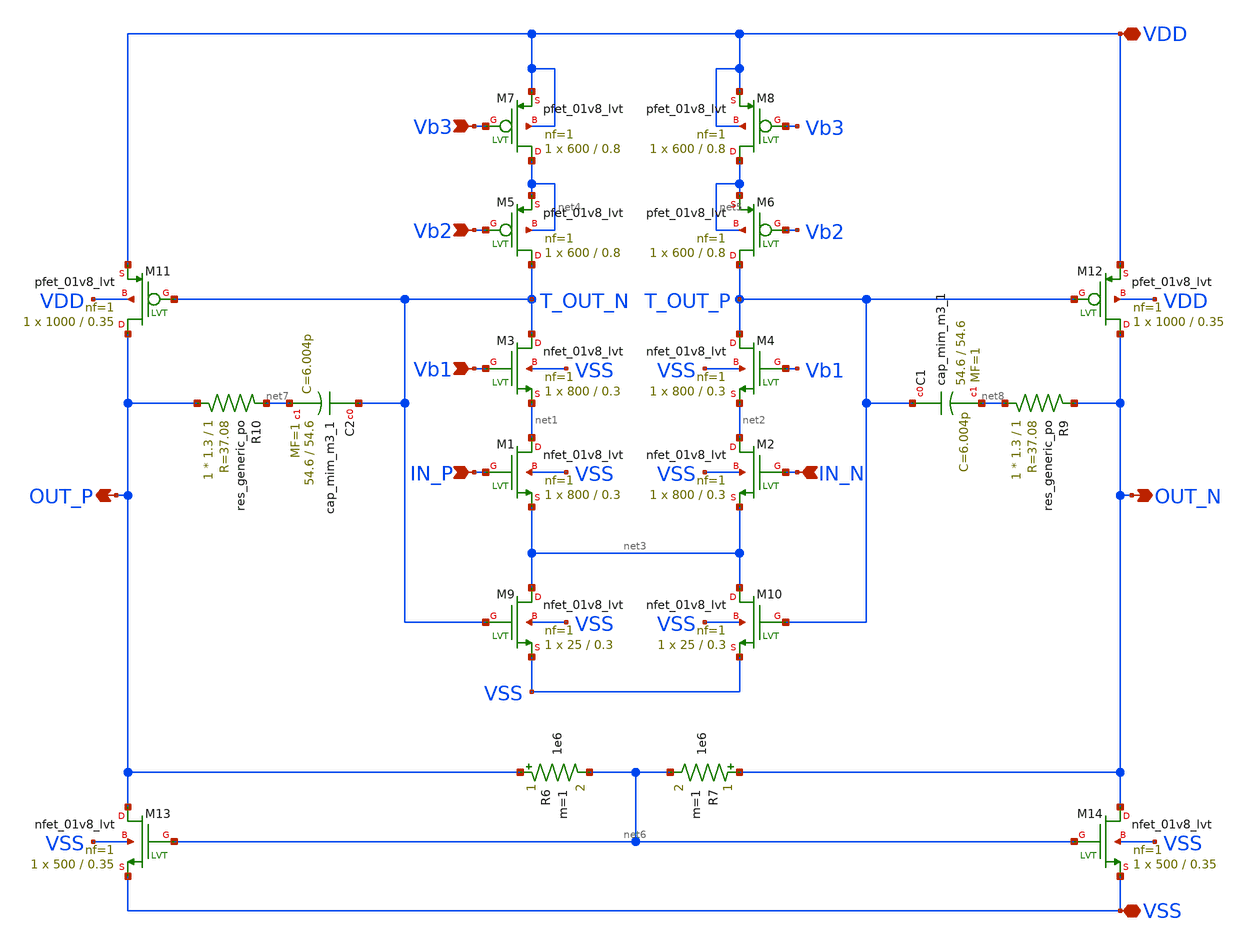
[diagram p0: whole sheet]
** sch_path: xschem/two_stage_amplifier.sch
**.subckt two_stage_amplifier VSS VDD Vb1 Vb2 Vb3 IN_P IN_N OUT_N OUT_P
*.iopin VSS
*.iopin VDD
*.ipin Vb1
*.ipin Vb2
*.ipin Vb3
*.ipin IN_P
*.ipin IN_N
*.opin OUT_N
*.opin OUT_P
XM1 net1 IN_P net3 VSS sky130_fd_pr__nfet_01v8_lvt L=0.3 W=800 nf=1 ad='int((1 + 1)/2) * 800 / 1 * 0.29'
+ as='int((1 + 2)/2) * 800 / 1 * 0.29' pd='2*int((1 + 1)/2) * (800 / 1 + 0.29)' ps='2*int((1 + 2)/2) * (800 / 1 + 0.29)'
+ nrd='0.29 / 800 ' nrs='0.29 / 800 ' sa=0 sb=0 sd=0 mult=1 m=1
XM2 net2 IN_N net3 VSS sky130_fd_pr__nfet_01v8_lvt L=0.3 W=800 nf=1 ad='int((1 + 1)/2) * 800 / 1 * 0.29'
+ as='int((1 + 2)/2) * 800 / 1 * 0.29' pd='2*int((1 + 1)/2) * (800 / 1 + 0.29)' ps='2*int((1 + 2)/2) * (800 / 1 + 0.29)'
+ nrd='0.29 / 800 ' nrs='0.29 / 800 ' sa=0 sb=0 sd=0 mult=1 m=1
XM3 T_OUT_N Vb1 net1 VSS sky130_fd_pr__nfet_01v8_lvt L=0.3 W=800 nf=1 ad='int((1 + 1)/2) * 800 / 1 * 0.29'
+ as='int((1 + 2)/2) * 800 / 1 * 0.29' pd='2*int((1 + 1)/2) * (800 / 1 + 0.29)' ps='2*int((1 + 2)/2) * (800 / 1 + 0.29)'
+ nrd='0.29 / 800 ' nrs='0.29 / 800 ' sa=0 sb=0 sd=0 mult=1 m=1
XM4 T_OUT_P Vb1 net2 VSS sky130_fd_pr__nfet_01v8_lvt L=0.3 W=800 nf=1 ad='int((1 + 1)/2) * 800 / 1 * 0.29'
+ as='int((1 + 2)/2) * 800 / 1 * 0.29' pd='2*int((1 + 1)/2) * (800 / 1 + 0.29)' ps='2*int((1 + 2)/2) * (800 / 1 + 0.29)'
+ nrd='0.29 / 800 ' nrs='0.29 / 800 ' sa=0 sb=0 sd=0 mult=1 m=1
XM5 T_OUT_N Vb2 net4 net4 sky130_fd_pr__pfet_01v8_lvt L=0.8 W=600 nf=1 ad='int((1 + 1)/2) * 600 / 1 * 0.29'
+ as='int((1 + 2)/2) * 600 / 1 * 0.29' pd='2*int((1 + 1)/2) * (600 / 1 + 0.29)' ps='2*int((1 + 2)/2) * (600 / 1 + 0.29)'
+ nrd='0.29 / 600 ' nrs='0.29 / 600 ' sa=0 sb=0 sd=0 mult=1 m=1
XM6 T_OUT_P Vb2 net5 net5 sky130_fd_pr__pfet_01v8_lvt L=0.8 W=600 nf=1 ad='int((1 + 1)/2) * 600 / 1 * 0.29'
+ as='int((1 + 2)/2) * 600 / 1 * 0.29' pd='2*int((1 + 1)/2) * (600 / 1 + 0.29)' ps='2*int((1 + 2)/2) * (600 / 1 + 0.29)'
+ nrd='0.29 / 600 ' nrs='0.29 / 600 ' sa=0 sb=0 sd=0 mult=1 m=1
XM7 net4 Vb3 VDD VDD sky130_fd_pr__pfet_01v8_lvt L=0.8 W=600 nf=1 ad='int((1 + 1)/2) * 600 / 1 * 0.29'
+ as='int((1 + 2)/2) * 600 / 1 * 0.29' pd='2*int((1 + 1)/2) * (600 / 1 + 0.29)' ps='2*int((1 + 2)/2) * (600 / 1 + 0.29)'
+ nrd='0.29 / 600 ' nrs='0.29 / 600 ' sa=0 sb=0 sd=0 mult=1 m=1
XM8 net5 Vb3 VDD VDD sky130_fd_pr__pfet_01v8_lvt L=0.8 W=600 nf=1 ad='int((1 + 1)/2) * 600 / 1 * 0.29'
+ as='int((1 + 2)/2) * 600 / 1 * 0.29' pd='2*int((1 + 1)/2) * (600 / 1 + 0.29)' ps='2*int((1 + 2)/2) * (600 / 1 + 0.29)'
+ nrd='0.29 / 600 ' nrs='0.29 / 600 ' sa=0 sb=0 sd=0 mult=1 m=1
XM9 net3 T_OUT_N VSS VSS sky130_fd_pr__nfet_01v8_lvt L=0.3 W=25 nf=1 ad='int((1 + 1)/2) * 25 / 1 * 0.29'
+ as='int((1 + 2)/2) * 25 / 1 * 0.29' pd='2*int((1 + 1)/2) * (25 / 1 + 0.29)' ps='2*int((1 + 2)/2) * (25 / 1 + 0.29)'
+ nrd='0.29 / 25 ' nrs='0.29 / 25 ' sa=0 sb=0 sd=0 mult=1 m=1
XM10 net3 T_OUT_P VSS VSS sky130_fd_pr__nfet_01v8_lvt L=0.3 W=25 nf=1 ad='int((1 + 1)/2) * 25 / 1 * 0.29'
+ as='int((1 + 2)/2) * 25 / 1 * 0.29' pd='2*int((1 + 1)/2) * (25 / 1 + 0.29)' ps='2*int((1 + 2)/2) * (25 / 1 + 0.29)'
+ nrd='0.29 / 25 ' nrs='0.29 / 25 ' sa=0 sb=0 sd=0 mult=1 m=1
XM12 OUT_N T_OUT_P VDD VDD sky130_fd_pr__pfet_01v8_lvt L=0.35 W=1000 nf=1 ad='int((1 + 1)/2) * 1000 / 1 * 0.29'
+ as='int((1 + 2)/2) * 1000 / 1 * 0.29' pd='2*int((1 + 1)/2) * (1000 / 1 + 0.29)' ps='2*int((1 + 2)/2) * (1000 / 1 + 0.29)'
+ nrd='0.29 / 1000 ' nrs='0.29 / 1000 ' sa=0 sb=0 sd=0 mult=1 m=1
XM11 OUT_P T_OUT_N VDD VDD sky130_fd_pr__pfet_01v8_lvt L=0.35 W=1000 nf=1 ad='int((1 + 1)/2) * 1000 / 1 * 0.29'
+ as='int((1 + 2)/2) * 1000 / 1 * 0.29' pd='2*int((1 + 1)/2) * (1000 / 1 + 0.29)' ps='2*int((1 + 2)/2) * (1000 / 1 + 0.29)'
+ nrd='0.29 / 1000 ' nrs='0.29 / 1000 ' sa=0 sb=0 sd=0 mult=1 m=1
XM14 OUT_N net6 VSS VSS sky130_fd_pr__nfet_01v8_lvt L=0.35 W=500 nf=1 ad='int((1 + 1)/2) * 500 / 1 * 0.29'
+ as='int((1 + 2)/2) * 500 / 1 * 0.29' pd='2*int((1 + 1)/2) * (500 / 1 + 0.29)' ps='2*int((1 + 2)/2) * (500 / 1 + 0.29)'
+ nrd='0.29 / 500 ' nrs='0.29 / 500 ' sa=0 sb=0 sd=0 mult=1 m=1
XM13 OUT_P net6 VSS VSS sky130_fd_pr__nfet_01v8_lvt L=0.35 W=500 nf=1 ad='int((1 + 1)/2) * 500 / 1 * 0.29'
+ as='int((1 + 2)/2) * 500 / 1 * 0.29' pd='2*int((1 + 1)/2) * (500 / 1 + 0.29)' ps='2*int((1 + 2)/2) * (500 / 1 + 0.29)'
+ nrd='0.29 / 500 ' nrs='0.29 / 500 ' sa=0 sb=0 sd=0 mult=1 m=1
R6 OUT_P net6 1e6 m=1
R7 OUT_N net6 1e6 m=1
XR10 OUT_P net7 sky130_fd_pr__res_generic_po W=1.3 L=1 m=1
XR9 net8 OUT_N sky130_fd_pr__res_generic_po W=1.3 L=1 m=1
XC2 T_OUT_N net7 sky130_fd_pr__cap_mim_m3_1 W=54.6 L=54.6 MF=1 m=1
XC1 T_OUT_P net8 sky130_fd_pr__cap_mim_m3_1 W=54.6 L=54.6 MF=1 m=1
**.ends
.end
